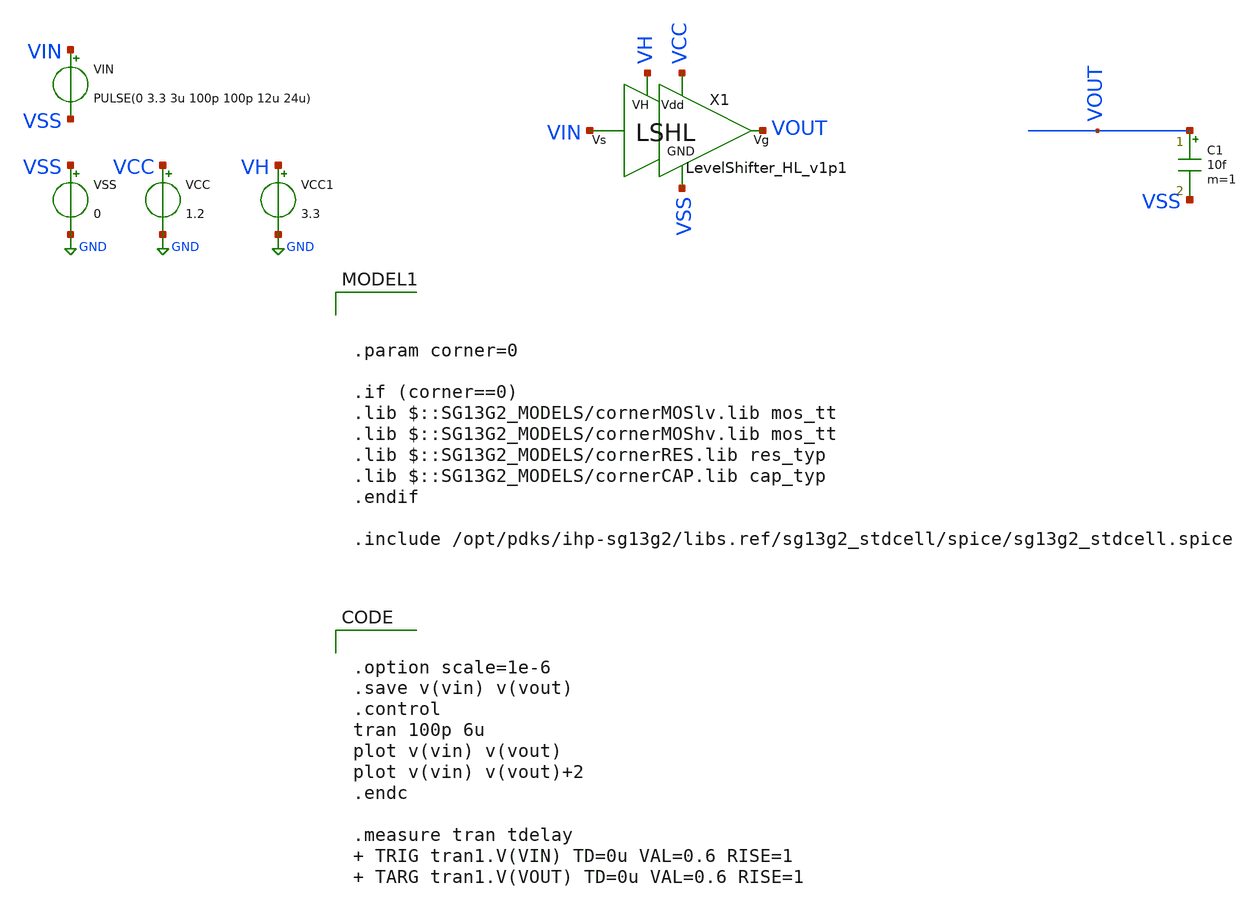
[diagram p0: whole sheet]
** sch_path: xschem/tb_LSHL_v1p1.sch
**.subckt tb_LSHL_v1p1
VCC VCC GND 1.2
VSS VSS GND 0
VIN VIN VSS PULSE(0 3.3 3u 100p 100p 12u 24u)
C1 VOUT VSS 10f m=1
X1 VIN VOUT VCC VH VSS LevelShifter_HL_v1p1
VCC1 VH GND 3.3
**** begin user architecture code


.option scale=1e-6
.save v(vin) v(vout)
.control
tran 100p 6u
plot v(vin) v(vout)
plot v(vin) v(vout)+2
.endc

.measure tran tdelay  TRIG tran1.V(VIN) TD=0u VAL=0.6 RISE=1  TARG tran1.V(VOUT) TD=0u VAL=0.6
+ RISE=1






.param corner=0

.if (corner==0)
.lib $::SG13G2_MODELS/cornerMOSlv.lib mos_tt
.lib $::SG13G2_MODELS/cornerMOShv.lib mos_tt
.lib $::SG13G2_MODELS/cornerRES.lib res_typ
.lib $::SG13G2_MODELS/cornerCAP.lib cap_typ
.endif

.include /opt/pdks/ihp-sg13g2/libs.ref/sg13g2_stdcell/spice/sg13g2_stdcell.spice

**** end user architecture code
**.ends

* expanding   symbol:  /home/designer/shared/TO202410_IHP_TDBuck/xschem/LevelShifter_HL_v1p1.sym #
*+ of pins=5
** sym_path: xschem/LevelShifter_HL_v1p1.sym
** sch_path: xschem/LevelShifter_HL_v1p1.sch
.subckt LevelShifter_HL_v1p1 Vs Vg Vdd VH GND
*.iopin VH
*.iopin Vdd
*.ipin Vs
*.opin Vg
*.iopin GND
XMD9 net1 Vg Vdd Vdd sg13_lv_pmos w=1u l=0.13u ng=1 m=2 mm_ok=1
XMD10 GND Vs net1 GND sg13_lv_nmos w=1u l=0.13u ng=1 m=1 mm_ok=1
XMD5 VgMD2 Vs VH VH sg13_hv_pmos w=1u l=0.4u ng=1 m=2 mm_ok=1
XMD6 GND Vs VgMD2 GND sg13_hv_nmos w=1u l=0.45u ng=1 m=1 mm_ok=1
XMD1 Vg net1 Vdd Vdd sg13_lv_pmos w=1u l=0.13u ng=1 m=2 mm_ok=1
XMD2 GND VgMD2 Vg GND sg13_lv_nmos w=1u l=0.13u ng=1 m=1 mm_ok=1
.ends

.GLOBAL GND
.end
